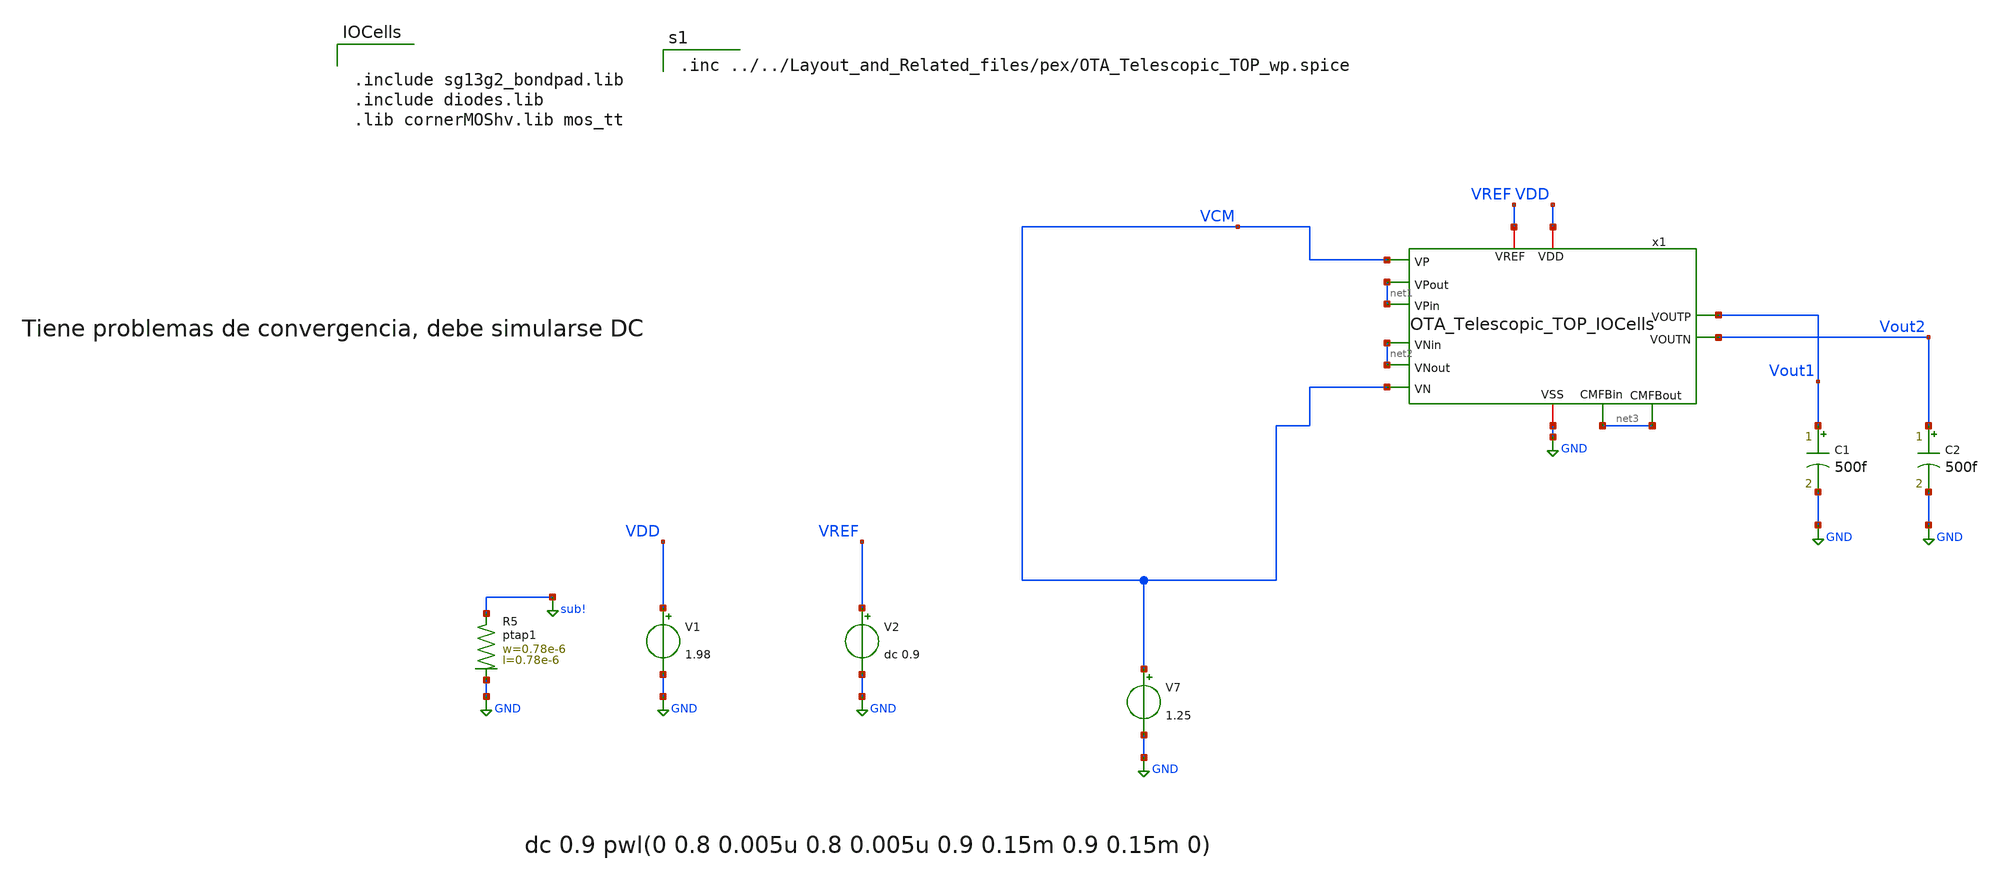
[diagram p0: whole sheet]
** sch_path: OTA_Telescopic/Testbenchs/OTA_Telescopic_TOP_TB_StartUp_io.sch
**.subckt OTA_Telescopic_TOP_TB_StartUp_io
V7 VCM GND 1.25
V1 VDD GND 1.98
V2 VREF GND dc 0.9
C1 Vout1 GND 500f m=1
C2 Vout2 GND 500f m=1
XR5 sub! GND ptap1 R=262.8 w=0.78e-6 l=0.78e-6
x1 VDD GND net1 VCM net1 Vout2 Vout1 net2 net2 VCM VREF net3 net3 OTA_Telescopic_TOP_IOCells
**** begin user architecture code

** opencircuitdesign pdks install
.lib cornerMOSlv.lib mos_ff
.lib cornerRES.lib res_typ
.lib cornerCAP.lib cap_typ
.temp 0



.include sg13g2_bondpad.lib
.include diodes.lib
.lib cornerMOShv.lib mos_tt





.control
 set color0 = white

set wr_singlescale
set wr_vecnames

save v(VDD) v(Vout1) v(Vout2) i(V1)
save v(x1.Vo1) v(x1.Vo2)

.options method=gear
tran 10p 500n
*write NMOS_diode_large_signal.raw

let VCM = v(Vout1)
let VDD = v(VDD)
let IDD = -i(V1)

wrdata VCM_tt_10ns_DC_io.txt VCM
wrdata IDD_tt_10ns_DC_io.txt IDD

plot VCM
plot VDD
plot IDD

let Vo1 = v(x1.Vo1)
let Vo2 = v(x1.Vo2)

let Vo = Vo1-Vo2

wrdata Vo Vo

.endc



.inc ../../Layout_and_Related_files/pex/OTA_Telescopic_TOP_wp.spice

**** end user architecture code
**.ends
.GLOBAL GND
.GLOBAL sub!
.end
